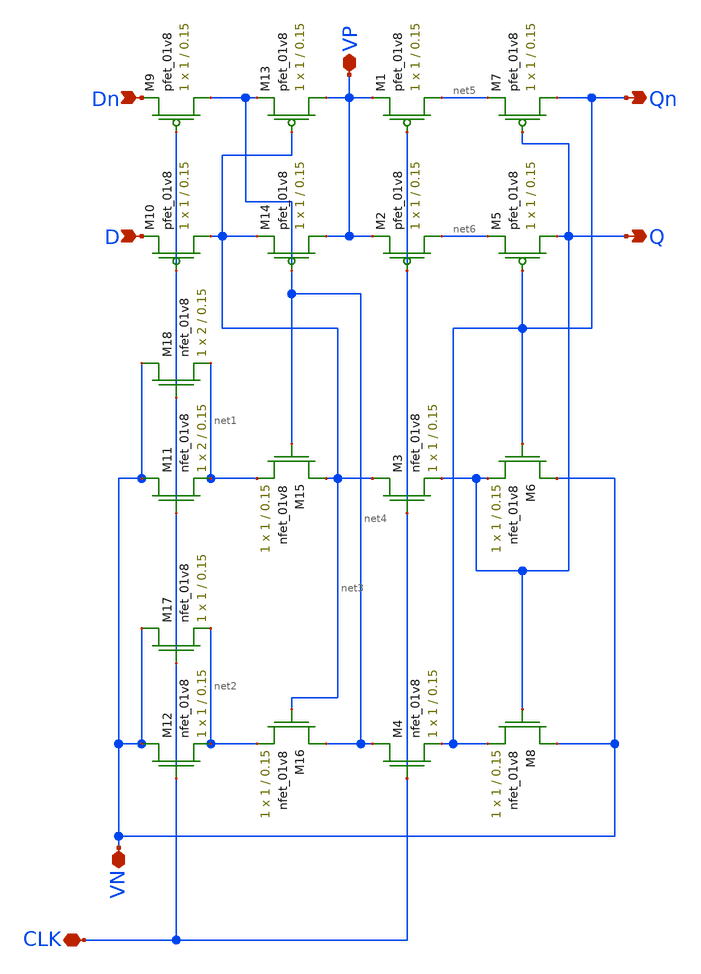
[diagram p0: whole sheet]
** sch_path: schematic/CSRL_D_FF.sch
**.subckt CSRL_D_FF Dn D VP VN CLK Qn Q
*.ipin Dn
*.ipin D
*.iopin VP
*.iopin VN
*.iopin CLK
*.opin Qn
*.opin Q
XM1 net5 CLK VP VDD sky130_fd_pr__pfet_01v8 L=0.15 W=1 nf=1 ad='int((nf+1)/2) * W/nf * 0.29' as='int((nf+2)/2) * W/nf * 0.29'
+ pd='2*int((nf+1)/2) * (W/nf + 0.29)' ps='2*int((nf+2)/2) * (W/nf + 0.29)' nrd='0.29 / W' nrs='0.29 / W'
+ sa=0 sb=0 sd=0 mult=1 m=1
XM2 net6 CLK VP VDD sky130_fd_pr__pfet_01v8 L=0.15 W=1 nf=1 ad='int((nf+1)/2) * W/nf * 0.29' as='int((nf+2)/2) * W/nf * 0.29'
+ pd='2*int((nf+1)/2) * (W/nf + 0.29)' ps='2*int((nf+2)/2) * (W/nf + 0.29)' nrd='0.29 / W' nrs='0.29 / W'
+ sa=0 sb=0 sd=0 mult=1 m=1
XM3 net3 CLK Q GND sky130_fd_pr__nfet_01v8 L=0.15 W=1 nf=1 ad='int((nf+1)/2) * W/nf * 0.29' as='int((nf+2)/2) * W/nf * 0.29'
+ pd='2*int((nf+1)/2) * (W/nf + 0.29)' ps='2*int((nf+2)/2) * (W/nf + 0.29)' nrd='0.29 / W' nrs='0.29 / W'
+ sa=0 sb=0 sd=0 mult=1 m=1
XM4 net4 CLK Qn GND sky130_fd_pr__nfet_01v8 L=0.15 W=1 nf=1 ad='int((nf+1)/2) * W/nf * 0.29' as='int((nf+2)/2) * W/nf * 0.29'
+ pd='2*int((nf+1)/2) * (W/nf + 0.29)' ps='2*int((nf+2)/2) * (W/nf + 0.29)' nrd='0.29 / W' nrs='0.29 / W'
+ sa=0 sb=0 sd=0 mult=1 m=1
XM5 Q Qn net6 VDD sky130_fd_pr__pfet_01v8 L=0.15 W=1 nf=1 ad='int((nf+1)/2) * W/nf * 0.29' as='int((nf+2)/2) * W/nf * 0.29'
+ pd='2*int((nf+1)/2) * (W/nf + 0.29)' ps='2*int((nf+2)/2) * (W/nf + 0.29)' nrd='0.29 / W' nrs='0.29 / W'
+ sa=0 sb=0 sd=0 mult=1 m=1
XM6 VN Qn Q GND sky130_fd_pr__nfet_01v8 L=0.15 W=1 nf=1 ad='int((nf+1)/2) * W/nf * 0.29' as='int((nf+2)/2) * W/nf * 0.29'
+ pd='2*int((nf+1)/2) * (W/nf + 0.29)' ps='2*int((nf+2)/2) * (W/nf + 0.29)' nrd='0.29 / W' nrs='0.29 / W'
+ sa=0 sb=0 sd=0 mult=1 m=1
XM7 Qn Q net5 VDD sky130_fd_pr__pfet_01v8 L=0.15 W=1 nf=1 ad='int((nf+1)/2) * W/nf * 0.29' as='int((nf+2)/2) * W/nf * 0.29'
+ pd='2*int((nf+1)/2) * (W/nf + 0.29)' ps='2*int((nf+2)/2) * (W/nf + 0.29)' nrd='0.29 / W' nrs='0.29 / W'
+ sa=0 sb=0 sd=0 mult=1 m=1
XM8 VN Q Qn GND sky130_fd_pr__nfet_01v8 L=0.15 W=1 nf=1 ad='int((nf+1)/2) * W/nf * 0.29' as='int((nf+2)/2) * W/nf * 0.29'
+ pd='2*int((nf+1)/2) * (W/nf + 0.29)' ps='2*int((nf+2)/2) * (W/nf + 0.29)' nrd='0.29 / W' nrs='0.29 / W'
+ sa=0 sb=0 sd=0 mult=1 m=1
XM9 net4 CLK Dn VDD sky130_fd_pr__pfet_01v8 L=0.15 W=1 nf=1 ad='int((nf+1)/2) * W/nf * 0.29' as='int((nf+2)/2) * W/nf * 0.29'
+ pd='2*int((nf+1)/2) * (W/nf + 0.29)' ps='2*int((nf+2)/2) * (W/nf + 0.29)' nrd='0.29 / W' nrs='0.29 / W'
+ sa=0 sb=0 sd=0 mult=1 m=1
XM10 net3 CLK D VDD sky130_fd_pr__pfet_01v8 L=0.15 W=1 nf=1 ad='int((nf+1)/2) * W/nf * 0.29' as='int((nf+2)/2) * W/nf * 0.29'
+ pd='2*int((nf+1)/2) * (W/nf + 0.29)' ps='2*int((nf+2)/2) * (W/nf + 0.29)' nrd='0.29 / W' nrs='0.29 / W'
+ sa=0 sb=0 sd=0 mult=1 m=1
XM11 VN CLK net1 GND sky130_fd_pr__nfet_01v8 L=0.15 W=2 nf=1 ad='int((nf+1)/2) * W/nf * 0.29' as='int((nf+2)/2) * W/nf * 0.29'
+ pd='2*int((nf+1)/2) * (W/nf + 0.29)' ps='2*int((nf+2)/2) * (W/nf + 0.29)' nrd='0.29 / W' nrs='0.29 / W'
+ sa=0 sb=0 sd=0 mult=1 m=1
XM12 VN CLK net2 GND sky130_fd_pr__nfet_01v8 L=0.15 W=1 nf=1 ad='int((nf+1)/2) * W/nf * 0.29' as='int((nf+2)/2) * W/nf * 0.29'
+ pd='2*int((nf+1)/2) * (W/nf + 0.29)' ps='2*int((nf+2)/2) * (W/nf + 0.29)' nrd='0.29 / W' nrs='0.29 / W'
+ sa=0 sb=0 sd=0 mult=1 m=1
XM13 VP net3 net4 VDD sky130_fd_pr__pfet_01v8 L=0.15 W=1 nf=1 ad='int((nf+1)/2) * W/nf * 0.29' as='int((nf+2)/2) * W/nf * 0.29'
+ pd='2*int((nf+1)/2) * (W/nf + 0.29)' ps='2*int((nf+2)/2) * (W/nf + 0.29)' nrd='0.29 / W' nrs='0.29 / W'
+ sa=0 sb=0 sd=0 mult=1 m=1
XM14 VP net4 net3 VDD sky130_fd_pr__pfet_01v8 L=0.15 W=1 nf=1 ad='int((nf+1)/2) * W/nf * 0.29' as='int((nf+2)/2) * W/nf * 0.29'
+ pd='2*int((nf+1)/2) * (W/nf + 0.29)' ps='2*int((nf+2)/2) * (W/nf + 0.29)' nrd='0.29 / W' nrs='0.29 / W'
+ sa=0 sb=0 sd=0 mult=1 m=1
XM15 net3 net4 net1 GND sky130_fd_pr__nfet_01v8 L=0.15 W=1 nf=1 ad='int((nf+1)/2) * W/nf * 0.29' as='int((nf+2)/2) * W/nf * 0.29'
+ pd='2*int((nf+1)/2) * (W/nf + 0.29)' ps='2*int((nf+2)/2) * (W/nf + 0.29)' nrd='0.29 / W' nrs='0.29 / W'
+ sa=0 sb=0 sd=0 mult=1 m=1
XM16 net4 net3 net2 GND sky130_fd_pr__nfet_01v8 L=0.15 W=1 nf=1 ad='int((nf+1)/2) * W/nf * 0.29' as='int((nf+2)/2) * W/nf * 0.29'
+ pd='2*int((nf+1)/2) * (W/nf + 0.29)' ps='2*int((nf+2)/2) * (W/nf + 0.29)' nrd='0.29 / W' nrs='0.29 / W'
+ sa=0 sb=0 sd=0 mult=1 m=1
XM17 VN CLK net2 GND sky130_fd_pr__nfet_01v8 L=0.15 W=1 nf=1 ad='int((nf+1)/2) * W/nf * 0.29' as='int((nf+2)/2) * W/nf * 0.29'
+ pd='2*int((nf+1)/2) * (W/nf + 0.29)' ps='2*int((nf+2)/2) * (W/nf + 0.29)' nrd='0.29 / W' nrs='0.29 / W'
+ sa=0 sb=0 sd=0 mult=1 m=1
XM18 VN CLK net1 GND sky130_fd_pr__nfet_01v8 L=0.15 W=2 nf=1 ad='int((nf+1)/2) * W/nf * 0.29' as='int((nf+2)/2) * W/nf * 0.29'
+ pd='2*int((nf+1)/2) * (W/nf + 0.29)' ps='2*int((nf+2)/2) * (W/nf + 0.29)' nrd='0.29 / W' nrs='0.29 / W'
+ sa=0 sb=0 sd=0 mult=1 m=1
**.ends
.end
